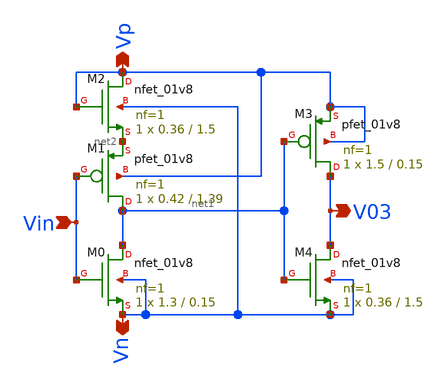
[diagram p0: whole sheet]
** sch_path: xschem/Vth_sch/Symbol/th03_backup.sch
**.subckt th03_backup Vn Vp Vin V03
*.opin Vn
*.opin Vp
*.ipin Vin
*.opin V03
XM3 V03 net1 Vp Vp sky130_fd_pr__pfet_01v8 L=0.15 W=1.5 nf=1 ad='int((nf+1)/2) * W/nf * 0.29' as='int((nf+2)/2) * W/nf * 0.29'
+ pd='2*int((nf+1)/2) * (W/nf + 0.29)' ps='2*int((nf+2)/2) * (W/nf + 0.29)' nrd='0.29 / W' nrs='0.29 / W'
+ sa=0 sb=0 sd=0 mult=1 m=1
XM4 V03 net1 Vn Vn sky130_fd_pr__nfet_01v8 L=1.5 W=0.36 nf=1 ad='int((nf+1)/2) * W/nf * 0.29' as='int((nf+2)/2) * W/nf * 0.29'
+ pd='2*int((nf+1)/2) * (W/nf + 0.29)' ps='2*int((nf+2)/2) * (W/nf + 0.29)' nrd='0.29 / W' nrs='0.29 / W'
+ sa=0 sb=0 sd=0 mult=1 m=1
XM1 net1 Vin net2 Vp sky130_fd_pr__pfet_01v8 L=1.39 W=0.42 nf=1 ad='int((nf+1)/2) * W/nf * 0.29' as='int((nf+2)/2) * W/nf * 0.29'
+ pd='2*int((nf+1)/2) * (W/nf + 0.29)' ps='2*int((nf+2)/2) * (W/nf + 0.29)' nrd='0.29 / W' nrs='0.29 / W'
+ sa=0 sb=0 sd=0 mult=1 m=1
XM0 net1 Vin Vn Vn sky130_fd_pr__nfet_01v8 L=0.15 W=1.3 nf=1 ad='int((nf+1)/2) * W/nf * 0.29' as='int((nf+2)/2) * W/nf * 0.29'
+ pd='2*int((nf+1)/2) * (W/nf + 0.29)' ps='2*int((nf+2)/2) * (W/nf + 0.29)' nrd='0.29 / W' nrs='0.29 / W'
+ sa=0 sb=0 sd=0 mult=1 m=1
XM2 Vp Vp net2 Vn sky130_fd_pr__nfet_01v8 L=1.5 W=0.36 nf=1 ad='int((nf+1)/2) * W/nf * 0.29' as='int((nf+2)/2) * W/nf * 0.29'
+ pd='2*int((nf+1)/2) * (W/nf + 0.29)' ps='2*int((nf+2)/2) * (W/nf + 0.29)' nrd='0.29 / W' nrs='0.29 / W'
+ sa=0 sb=0 sd=0 mult=1 m=1
**.ends
.end
